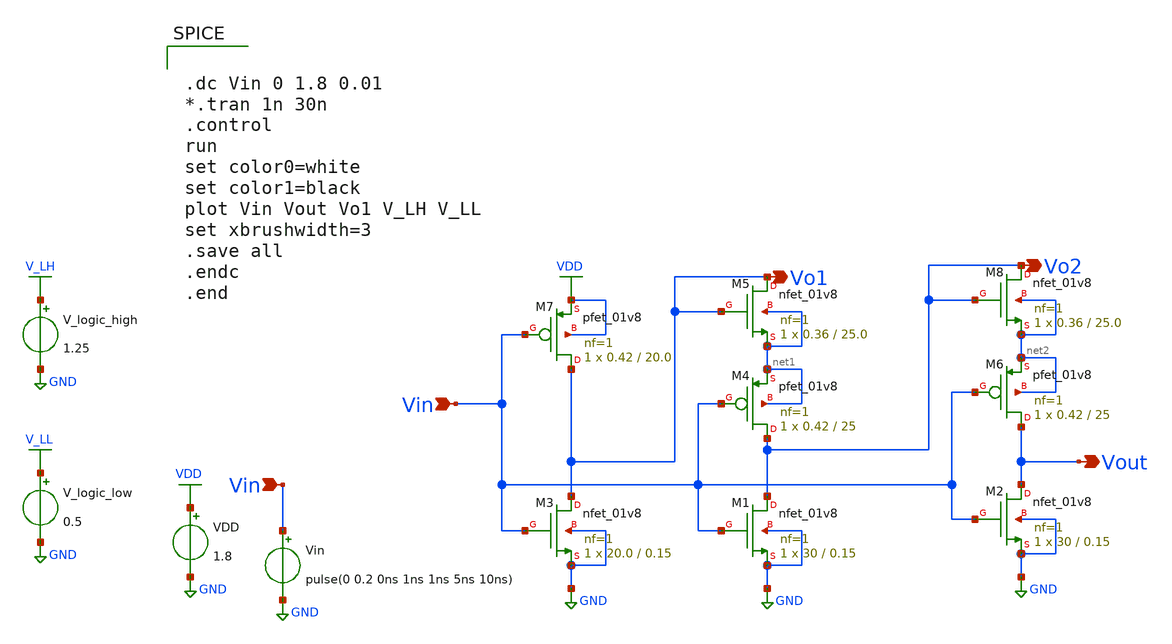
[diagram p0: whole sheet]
** sch_path: xschem/Vth_sch/Inverter-th2.sch
**.subckt Inverter-th2 Vin Vin Vo1 Vout Vo2
*.ipin Vin
*.ipin Vin
*.opin Vo1
*.opin Vout
*.opin Vo2
VDD VDD GND 1.8
Vin Vin GND pulse(0 0.2 0ns 1ns 1ns 5ns 10ns)
V_logic_high V_LH GND 1.25
V_logic_low V_LL GND 0.5
XM3 Vo1 Vin GND GND sky130_fd_pr__nfet_01v8 L=0.15 W=20.0 nf=1 ad='int((nf+1)/2) * W/nf * 0.29' as='int((nf+2)/2) * W/nf * 0.29'
+ pd='2*int((nf+1)/2) * (W/nf + 0.29)' ps='2*int((nf+2)/2) * (W/nf + 0.29)' nrd='0.29 / W' nrs='0.29 / W'
+ sa=0 sb=0 sd=0 mult=1 m=1
XM1 Vo2 Vin GND GND sky130_fd_pr__nfet_01v8 L=0.15 W=30 nf=1 ad='int((nf+1)/2) * W/nf * 0.29' as='int((nf+2)/2) * W/nf * 0.29'
+ pd='2*int((nf+1)/2) * (W/nf + 0.29)' ps='2*int((nf+2)/2) * (W/nf + 0.29)' nrd='0.29 / W' nrs='0.29 / W'
+ sa=0 sb=0 sd=0 mult=1 m=1
XM4 Vo2 Vin net1 net1 sky130_fd_pr__pfet_01v8 L=25 W=0.42 nf=1 ad='int((nf+1)/2) * W/nf * 0.29' as='int((nf+2)/2) * W/nf * 0.29'
+ pd='2*int((nf+1)/2) * (W/nf + 0.29)' ps='2*int((nf+2)/2) * (W/nf + 0.29)' nrd='0.29 / W' nrs='0.29 / W'
+ sa=0 sb=0 sd=0 mult=1 m=1
XM5 Vo1 Vo1 net1 net1 sky130_fd_pr__nfet_01v8 L=25.0 W=0.36 nf=1 ad='int((nf+1)/2) * W/nf * 0.29' as='int((nf+2)/2) * W/nf * 0.29'
+ pd='2*int((nf+1)/2) * (W/nf + 0.29)' ps='2*int((nf+2)/2) * (W/nf + 0.29)' nrd='0.29 / W' nrs='0.29 / W'
+ sa=0 sb=0 sd=0 mult=1 m=1
XM7 Vo1 Vin VDD VDD sky130_fd_pr__pfet_01v8 L=20.0 W=0.42 nf=1 ad='int((nf+1)/2) * W/nf * 0.29' as='int((nf+2)/2) * W/nf * 0.29'
+ pd='2*int((nf+1)/2) * (W/nf + 0.29)' ps='2*int((nf+2)/2) * (W/nf + 0.29)' nrd='0.29 / W' nrs='0.29 / W'
+ sa=0 sb=0 sd=0 mult=1 m=1
XM2 Vout Vin GND GND sky130_fd_pr__nfet_01v8 L=0.15 W=30 nf=1 ad='int((nf+1)/2) * W/nf * 0.29' as='int((nf+2)/2) * W/nf * 0.29'
+ pd='2*int((nf+1)/2) * (W/nf + 0.29)' ps='2*int((nf+2)/2) * (W/nf + 0.29)' nrd='0.29 / W' nrs='0.29 / W'
+ sa=0 sb=0 sd=0 mult=1 m=1
XM6 Vout Vin net2 net2 sky130_fd_pr__pfet_01v8 L=25 W=0.42 nf=1 ad='int((nf+1)/2) * W/nf * 0.29' as='int((nf+2)/2) * W/nf * 0.29'
+ pd='2*int((nf+1)/2) * (W/nf + 0.29)' ps='2*int((nf+2)/2) * (W/nf + 0.29)' nrd='0.29 / W' nrs='0.29 / W'
+ sa=0 sb=0 sd=0 mult=1 m=1
XM8 Vo2 Vo2 net2 net2 sky130_fd_pr__nfet_01v8 L=25.0 W=0.36 nf=1 ad='int((nf+1)/2) * W/nf * 0.29' as='int((nf+2)/2) * W/nf * 0.29'
+ pd='2*int((nf+1)/2) * (W/nf + 0.29)' ps='2*int((nf+2)/2) * (W/nf + 0.29)' nrd='0.29 / W' nrs='0.29 / W'
+ sa=0 sb=0 sd=0 mult=1 m=1
**** begin user architecture code


.lib /usr/local/share/pdk/sky130A/libs.tech/ngspice/sky130.lib.spice tt

.save all





.dc Vin 0 1.8 0.01
*.tran 1n 30n
.control
run
set color0=white
set color1=black
plot Vin Vout Vo1 V_LH V_LL
set xbrushwidth=3
.save all
.endc
.end


**** end user architecture code
**.ends
.GLOBAL VDD
.GLOBAL GND
.GLOBAL V_LH
.GLOBAL V_LL
.end
